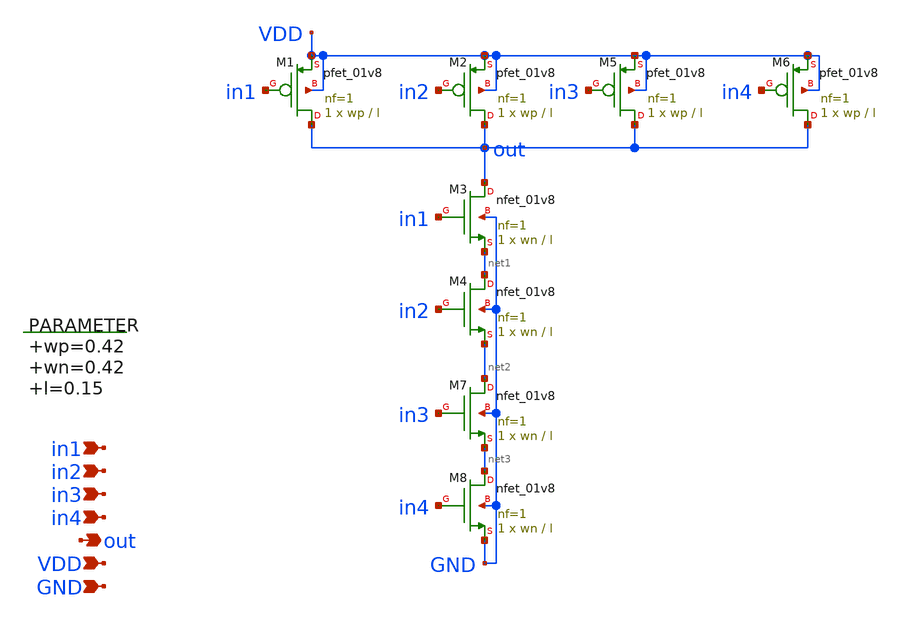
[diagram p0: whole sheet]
** sch_path: xschem/nand_4in.sch
**.subckt nand_4in in2 out VDD GND in1 in4 in3
*.ipin in2
*.opin out
*.ipin VDD
*.ipin GND
*.ipin in1
*.ipin in4
*.ipin in3
.param wp=0.42 wn=0.42 l=0.15
XM1 out in1 VDD VDD sky130_fd_pr__pfet_01v8 L=l W=wp nf=1 ad='int((nf+1)/2) * W/nf * 0.29' as='int((nf+2)/2) * W/nf * 0.29'
+ pd='2*int((nf+1)/2) * (W/nf + 0.29)' ps='2*int((nf+2)/2) * (W/nf + 0.29)' nrd='0.29 / W' nrs='0.29 / W'
+ sa=0 sb=0 sd=0 mult=1 m=1
XM2 out in2 VDD VDD sky130_fd_pr__pfet_01v8 L=l W=wp nf=1 ad='int((nf+1)/2) * W/nf * 0.29' as='int((nf+2)/2) * W/nf * 0.29'
+ pd='2*int((nf+1)/2) * (W/nf + 0.29)' ps='2*int((nf+2)/2) * (W/nf + 0.29)' nrd='0.29 / W' nrs='0.29 / W'
+ sa=0 sb=0 sd=0 mult=1 m=1
XM3 out in1 net1 GND sky130_fd_pr__nfet_01v8 L=l W=wn nf=1 ad='int((nf+1)/2) * W/nf * 0.29' as='int((nf+2)/2) * W/nf * 0.29'
+ pd='2*int((nf+1)/2) * (W/nf + 0.29)' ps='2*int((nf+2)/2) * (W/nf + 0.29)' nrd='0.29 / W' nrs='0.29 / W'
+ sa=0 sb=0 sd=0 mult=1 m=1
XM4 net1 in2 net2 GND sky130_fd_pr__nfet_01v8 L=l W=wn nf=1 ad='int((nf+1)/2) * W/nf * 0.29' as='int((nf+2)/2) * W/nf * 0.29'
+ pd='2*int((nf+1)/2) * (W/nf + 0.29)' ps='2*int((nf+2)/2) * (W/nf + 0.29)' nrd='0.29 / W' nrs='0.29 / W'
+ sa=0 sb=0 sd=0 mult=1 m=1
XM5 out in3 VDD VDD sky130_fd_pr__pfet_01v8 L=l W=wp nf=1 ad='int((nf+1)/2) * W/nf * 0.29' as='int((nf+2)/2) * W/nf * 0.29'
+ pd='2*int((nf+1)/2) * (W/nf + 0.29)' ps='2*int((nf+2)/2) * (W/nf + 0.29)' nrd='0.29 / W' nrs='0.29 / W'
+ sa=0 sb=0 sd=0 mult=1 m=1
XM6 out in4 VDD VDD sky130_fd_pr__pfet_01v8 L=l W=wp nf=1 ad='int((nf+1)/2) * W/nf * 0.29' as='int((nf+2)/2) * W/nf * 0.29'
+ pd='2*int((nf+1)/2) * (W/nf + 0.29)' ps='2*int((nf+2)/2) * (W/nf + 0.29)' nrd='0.29 / W' nrs='0.29 / W'
+ sa=0 sb=0 sd=0 mult=1 m=1
XM7 net2 in3 net3 GND sky130_fd_pr__nfet_01v8 L=l W=wn nf=1 ad='int((nf+1)/2) * W/nf * 0.29' as='int((nf+2)/2) * W/nf * 0.29'
+ pd='2*int((nf+1)/2) * (W/nf + 0.29)' ps='2*int((nf+2)/2) * (W/nf + 0.29)' nrd='0.29 / W' nrs='0.29 / W'
+ sa=0 sb=0 sd=0 mult=1 m=1
XM8 net3 in4 GND GND sky130_fd_pr__nfet_01v8 L=l W=wn nf=1 ad='int((nf+1)/2) * W/nf * 0.29' as='int((nf+2)/2) * W/nf * 0.29'
+ pd='2*int((nf+1)/2) * (W/nf + 0.29)' ps='2*int((nf+2)/2) * (W/nf + 0.29)' nrd='0.29 / W' nrs='0.29 / W'
+ sa=0 sb=0 sd=0 mult=1 m=1
**.ends
.end
